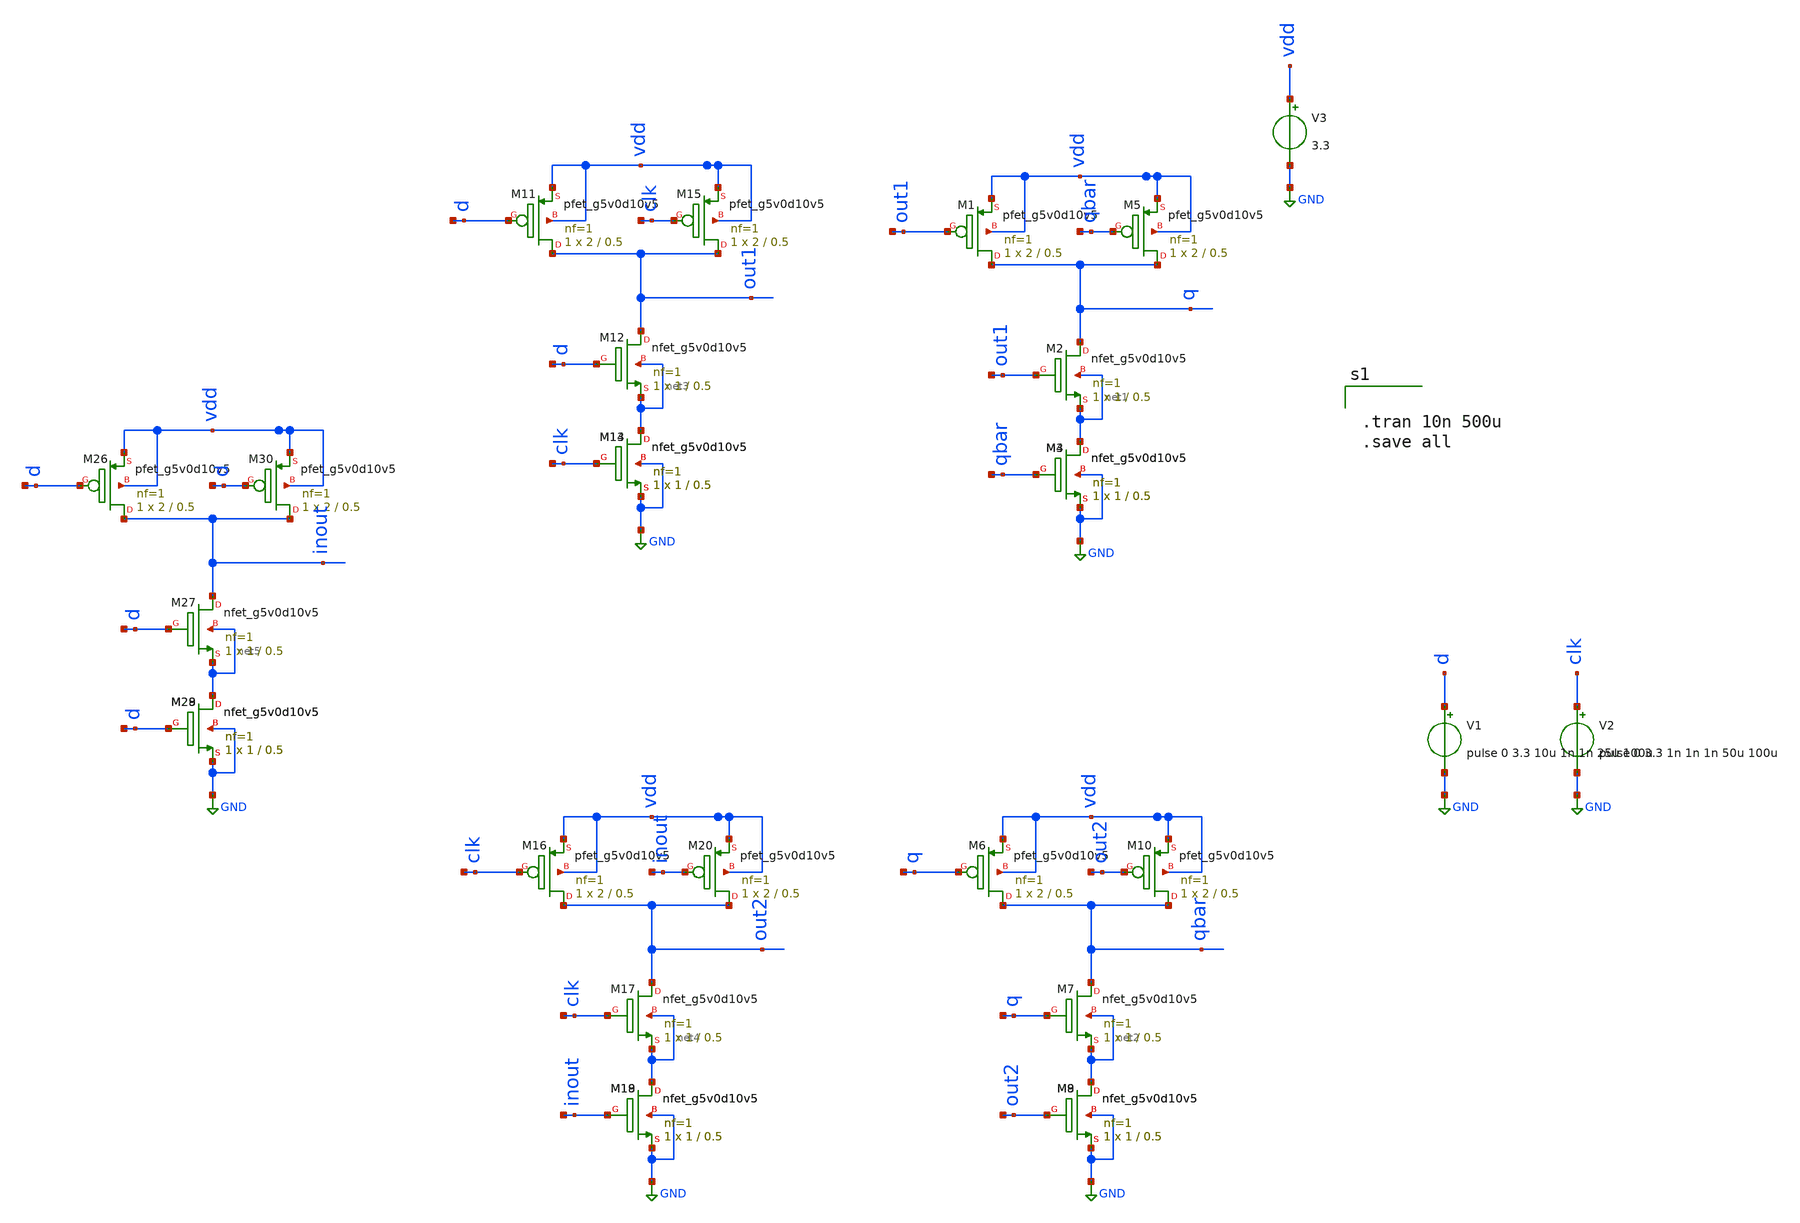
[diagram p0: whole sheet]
** sch_path: xschem/FDC/nand_gate.sch
**.subckt nand_gate
XM1 q out1 vdd vdd sky130_fd_pr__pfet_g5v0d10v5 L=0.5 W=2 nf=1 ad='int((nf+1)/2) * W/nf * 0.29' as='int((nf+2)/2) * W/nf * 0.29'
+ pd='2*int((nf+1)/2) * (W/nf + 0.29)' ps='2*int((nf+2)/2) * (W/nf + 0.29)' nrd='0.29 / W' nrs='0.29 / W'
+ sa=0 sb=0 sd=0 mult=1 m=1
XM2 q out1 net1 net1 sky130_fd_pr__nfet_g5v0d10v5 L=0.5 W=1 nf=1 ad='int((nf+1)/2) * W/nf * 0.29' as='int((nf+2)/2) * W/nf * 0.29'
+ pd='2*int((nf+1)/2) * (W/nf + 0.29)' ps='2*int((nf+2)/2) * (W/nf + 0.29)' nrd='0.29 / W' nrs='0.29 / W'
+ sa=0 sb=0 sd=0 mult=1 m=1
XM3 net1 qbar GND GND sky130_fd_pr__nfet_g5v0d10v5 L=0.5 W=1 nf=1 ad='int((nf+1)/2) * W/nf * 0.29' as='int((nf+2)/2) * W/nf * 0.29'
+ pd='2*int((nf+1)/2) * (W/nf + 0.29)' ps='2*int((nf+2)/2) * (W/nf + 0.29)' nrd='0.29 / W' nrs='0.29 / W'
+ sa=0 sb=0 sd=0 mult=1 m=1
XM4 net1 qbar GND GND sky130_fd_pr__nfet_g5v0d10v5 L=0.5 W=1 nf=1 ad='int((nf+1)/2) * W/nf * 0.29' as='int((nf+2)/2) * W/nf * 0.29'
+ pd='2*int((nf+1)/2) * (W/nf + 0.29)' ps='2*int((nf+2)/2) * (W/nf + 0.29)' nrd='0.29 / W' nrs='0.29 / W'
+ sa=0 sb=0 sd=0 mult=1 m=1
XM5 q qbar vdd vdd sky130_fd_pr__pfet_g5v0d10v5 L=0.5 W=2 nf=1 ad='int((nf+1)/2) * W/nf * 0.29' as='int((nf+2)/2) * W/nf * 0.29'
+ pd='2*int((nf+1)/2) * (W/nf + 0.29)' ps='2*int((nf+2)/2) * (W/nf + 0.29)' nrd='0.29 / W' nrs='0.29 / W'
+ sa=0 sb=0 sd=0 mult=1 m=1
XM6 qbar q vdd vdd sky130_fd_pr__pfet_g5v0d10v5 L=0.5 W=2 nf=1 ad='int((nf+1)/2) * W/nf * 0.29' as='int((nf+2)/2) * W/nf * 0.29'
+ pd='2*int((nf+1)/2) * (W/nf + 0.29)' ps='2*int((nf+2)/2) * (W/nf + 0.29)' nrd='0.29 / W' nrs='0.29 / W'
+ sa=0 sb=0 sd=0 mult=1 m=1
XM7 qbar q net2 net2 sky130_fd_pr__nfet_g5v0d10v5 L=0.5 W=1 nf=1 ad='int((nf+1)/2) * W/nf * 0.29' as='int((nf+2)/2) * W/nf * 0.29'
+ pd='2*int((nf+1)/2) * (W/nf + 0.29)' ps='2*int((nf+2)/2) * (W/nf + 0.29)' nrd='0.29 / W' nrs='0.29 / W'
+ sa=0 sb=0 sd=0 mult=1 m=1
XM8 net2 out2 GND GND sky130_fd_pr__nfet_g5v0d10v5 L=0.5 W=1 nf=1 ad='int((nf+1)/2) * W/nf * 0.29' as='int((nf+2)/2) * W/nf * 0.29'
+ pd='2*int((nf+1)/2) * (W/nf + 0.29)' ps='2*int((nf+2)/2) * (W/nf + 0.29)' nrd='0.29 / W' nrs='0.29 / W'
+ sa=0 sb=0 sd=0 mult=1 m=1
XM9 net2 out2 GND GND sky130_fd_pr__nfet_g5v0d10v5 L=0.5 W=1 nf=1 ad='int((nf+1)/2) * W/nf * 0.29' as='int((nf+2)/2) * W/nf * 0.29'
+ pd='2*int((nf+1)/2) * (W/nf + 0.29)' ps='2*int((nf+2)/2) * (W/nf + 0.29)' nrd='0.29 / W' nrs='0.29 / W'
+ sa=0 sb=0 sd=0 mult=1 m=1
XM10 qbar out2 vdd vdd sky130_fd_pr__pfet_g5v0d10v5 L=0.5 W=2 nf=1 ad='int((nf+1)/2) * W/nf * 0.29' as='int((nf+2)/2) * W/nf * 0.29'
+ pd='2*int((nf+1)/2) * (W/nf + 0.29)' ps='2*int((nf+2)/2) * (W/nf + 0.29)' nrd='0.29 / W' nrs='0.29 / W'
+ sa=0 sb=0 sd=0 mult=1 m=1
V3 vdd GND 3.3
XM11 out1 d vdd vdd sky130_fd_pr__pfet_g5v0d10v5 L=0.5 W=2 nf=1 ad='int((nf+1)/2) * W/nf * 0.29' as='int((nf+2)/2) * W/nf * 0.29'
+ pd='2*int((nf+1)/2) * (W/nf + 0.29)' ps='2*int((nf+2)/2) * (W/nf + 0.29)' nrd='0.29 / W' nrs='0.29 / W'
+ sa=0 sb=0 sd=0 mult=1 m=1
XM12 out1 d net3 net3 sky130_fd_pr__nfet_g5v0d10v5 L=0.5 W=1 nf=1 ad='int((nf+1)/2) * W/nf * 0.29' as='int((nf+2)/2) * W/nf * 0.29'
+ pd='2*int((nf+1)/2) * (W/nf + 0.29)' ps='2*int((nf+2)/2) * (W/nf + 0.29)' nrd='0.29 / W' nrs='0.29 / W'
+ sa=0 sb=0 sd=0 mult=1 m=1
XM13 net3 clk GND GND sky130_fd_pr__nfet_g5v0d10v5 L=0.5 W=1 nf=1 ad='int((nf+1)/2) * W/nf * 0.29' as='int((nf+2)/2) * W/nf * 0.29'
+ pd='2*int((nf+1)/2) * (W/nf + 0.29)' ps='2*int((nf+2)/2) * (W/nf + 0.29)' nrd='0.29 / W' nrs='0.29 / W'
+ sa=0 sb=0 sd=0 mult=1 m=1
XM14 net3 clk GND GND sky130_fd_pr__nfet_g5v0d10v5 L=0.5 W=1 nf=1 ad='int((nf+1)/2) * W/nf * 0.29' as='int((nf+2)/2) * W/nf * 0.29'
+ pd='2*int((nf+1)/2) * (W/nf + 0.29)' ps='2*int((nf+2)/2) * (W/nf + 0.29)' nrd='0.29 / W' nrs='0.29 / W'
+ sa=0 sb=0 sd=0 mult=1 m=1
XM15 out1 clk vdd vdd sky130_fd_pr__pfet_g5v0d10v5 L=0.5 W=2 nf=1 ad='int((nf+1)/2) * W/nf * 0.29' as='int((nf+2)/2) * W/nf * 0.29'
+ pd='2*int((nf+1)/2) * (W/nf + 0.29)' ps='2*int((nf+2)/2) * (W/nf + 0.29)' nrd='0.29 / W' nrs='0.29 / W'
+ sa=0 sb=0 sd=0 mult=1 m=1
XM16 out2 clk vdd vdd sky130_fd_pr__pfet_g5v0d10v5 L=0.5 W=2 nf=1 ad='int((nf+1)/2) * W/nf * 0.29' as='int((nf+2)/2) * W/nf * 0.29'
+ pd='2*int((nf+1)/2) * (W/nf + 0.29)' ps='2*int((nf+2)/2) * (W/nf + 0.29)' nrd='0.29 / W' nrs='0.29 / W'
+ sa=0 sb=0 sd=0 mult=1 m=1
XM17 out2 clk net4 net4 sky130_fd_pr__nfet_g5v0d10v5 L=0.5 W=1 nf=1 ad='int((nf+1)/2) * W/nf * 0.29'
+ as='int((nf+2)/2) * W/nf * 0.29' pd='2*int((nf+1)/2) * (W/nf + 0.29)' ps='2*int((nf+2)/2) * (W/nf + 0.29)'
+ nrd='0.29 / W' nrs='0.29 / W' sa=0 sb=0 sd=0 mult=1 m=1
XM18 net4 inout GND GND sky130_fd_pr__nfet_g5v0d10v5 L=0.5 W=1 nf=1 ad='int((nf+1)/2) * W/nf * 0.29'
+ as='int((nf+2)/2) * W/nf * 0.29' pd='2*int((nf+1)/2) * (W/nf + 0.29)' ps='2*int((nf+2)/2) * (W/nf + 0.29)'
+ nrd='0.29 / W' nrs='0.29 / W' sa=0 sb=0 sd=0 mult=1 m=1
XM19 net4 inout GND GND sky130_fd_pr__nfet_g5v0d10v5 L=0.5 W=1 nf=1 ad='int((nf+1)/2) * W/nf * 0.29'
+ as='int((nf+2)/2) * W/nf * 0.29' pd='2*int((nf+1)/2) * (W/nf + 0.29)' ps='2*int((nf+2)/2) * (W/nf + 0.29)'
+ nrd='0.29 / W' nrs='0.29 / W' sa=0 sb=0 sd=0 mult=1 m=1
XM20 out2 inout vdd vdd sky130_fd_pr__pfet_g5v0d10v5 L=0.5 W=2 nf=1 ad='int((nf+1)/2) * W/nf * 0.29'
+ as='int((nf+2)/2) * W/nf * 0.29' pd='2*int((nf+1)/2) * (W/nf + 0.29)' ps='2*int((nf+2)/2) * (W/nf + 0.29)'
+ nrd='0.29 / W' nrs='0.29 / W' sa=0 sb=0 sd=0 mult=1 m=1
XM26 inout d vdd vdd sky130_fd_pr__pfet_g5v0d10v5 L=0.5 W=2 nf=1 ad='int((nf+1)/2) * W/nf * 0.29' as='int((nf+2)/2) * W/nf * 0.29'
+ pd='2*int((nf+1)/2) * (W/nf + 0.29)' ps='2*int((nf+2)/2) * (W/nf + 0.29)' nrd='0.29 / W' nrs='0.29 / W'
+ sa=0 sb=0 sd=0 mult=1 m=1
XM27 inout d net5 net5 sky130_fd_pr__nfet_g5v0d10v5 L=0.5 W=1 nf=1 ad='int((nf+1)/2) * W/nf * 0.29' as='int((nf+2)/2) * W/nf * 0.29'
+ pd='2*int((nf+1)/2) * (W/nf + 0.29)' ps='2*int((nf+2)/2) * (W/nf + 0.29)' nrd='0.29 / W' nrs='0.29 / W'
+ sa=0 sb=0 sd=0 mult=1 m=1
XM28 net5 d GND GND sky130_fd_pr__nfet_g5v0d10v5 L=0.5 W=1 nf=1 ad='int((nf+1)/2) * W/nf * 0.29' as='int((nf+2)/2) * W/nf * 0.29'
+ pd='2*int((nf+1)/2) * (W/nf + 0.29)' ps='2*int((nf+2)/2) * (W/nf + 0.29)' nrd='0.29 / W' nrs='0.29 / W'
+ sa=0 sb=0 sd=0 mult=1 m=1
XM29 net5 d GND GND sky130_fd_pr__nfet_g5v0d10v5 L=0.5 W=1 nf=1 ad='int((nf+1)/2) * W/nf * 0.29' as='int((nf+2)/2) * W/nf * 0.29'
+ pd='2*int((nf+1)/2) * (W/nf + 0.29)' ps='2*int((nf+2)/2) * (W/nf + 0.29)' nrd='0.29 / W' nrs='0.29 / W'
+ sa=0 sb=0 sd=0 mult=1 m=1
XM30 inout d vdd vdd sky130_fd_pr__pfet_g5v0d10v5 L=0.5 W=2 nf=1 ad='int((nf+1)/2) * W/nf * 0.29' as='int((nf+2)/2) * W/nf * 0.29'
+ pd='2*int((nf+1)/2) * (W/nf + 0.29)' ps='2*int((nf+2)/2) * (W/nf + 0.29)' nrd='0.29 / W' nrs='0.29 / W'
+ sa=0 sb=0 sd=0 mult=1 m=1
V1 d GND pulse 0 3.3 10u 1n 1n 25u 100u
V2 clk GND pulse 0 3.3 1n 1n 1n 50u 100u
**** begin user architecture code
  .lib /home/vinodhini/open_pdks/sky130/sky130A/libs.tech/ngspice/sky130.lib.spice tt


.tran 10n 500u
.save all

**** end user architecture code
**.ends
.GLOBAL GND
.end
